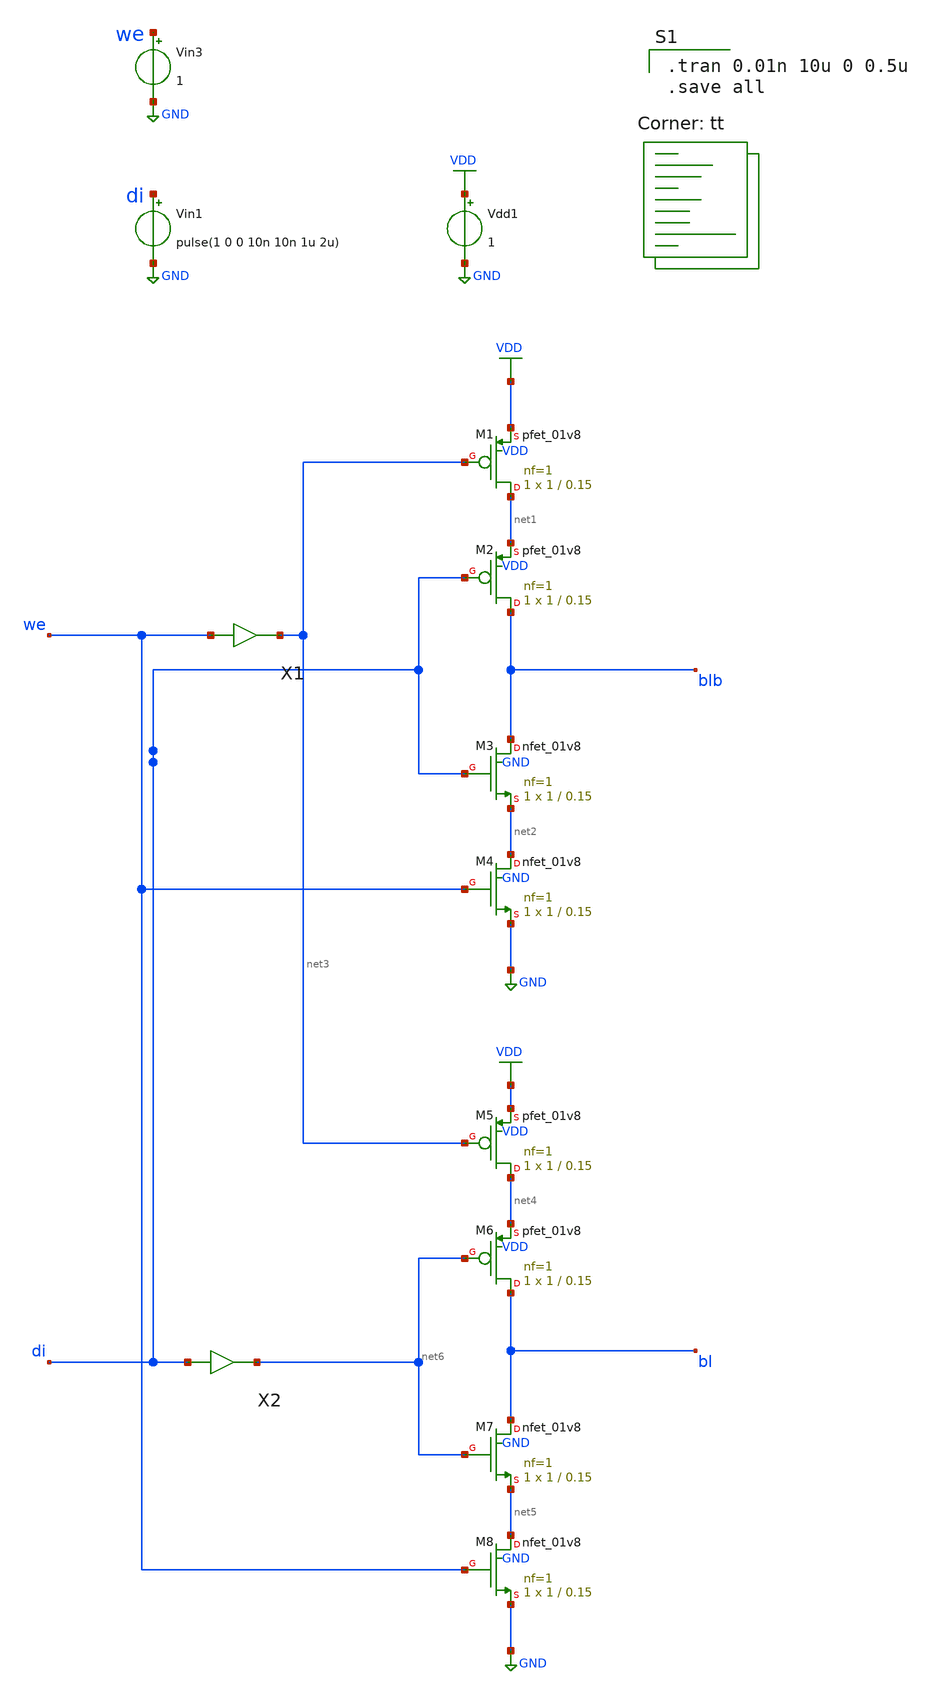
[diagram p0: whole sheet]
** sch_path: gates/Memory/write drive sim.sch
**.subckt write drive sim
X1 we net3 inv_vtc
X2 di net6 inv_vtc
XM1 net1 net3 VDD VDD sky130_fd_pr__pfet_01v8 L=0.15 W=1 nf=1 ad='int((nf+1)/2) * W/nf * 0.29' as='int((nf+2)/2) * W/nf * 0.29'
+ pd='2*int((nf+1)/2) * (W/nf + 0.29)' ps='2*int((nf+2)/2) * (W/nf + 0.29)' nrd='0.29 / W' nrs='0.29 / W'
+ sa=0 sb=0 sd=0 mult=1 m=1
XM2 blb di net1 VDD sky130_fd_pr__pfet_01v8 L=0.15 W=1 nf=1 ad='int((nf+1)/2) * W/nf * 0.29' as='int((nf+2)/2) * W/nf * 0.29'
+ pd='2*int((nf+1)/2) * (W/nf + 0.29)' ps='2*int((nf+2)/2) * (W/nf + 0.29)' nrd='0.29 / W' nrs='0.29 / W'
+ sa=0 sb=0 sd=0 mult=1 m=1
XM3 blb di net2 GND sky130_fd_pr__nfet_01v8 L=0.15 W=1 nf=1 ad='int((nf+1)/2) * W/nf * 0.29' as='int((nf+2)/2) * W/nf * 0.29'
+ pd='2*int((nf+1)/2) * (W/nf + 0.29)' ps='2*int((nf+2)/2) * (W/nf + 0.29)' nrd='0.29 / W' nrs='0.29 / W'
+ sa=0 sb=0 sd=0 mult=1 m=1
XM4 net2 we GND GND sky130_fd_pr__nfet_01v8 L=0.15 W=1 nf=1 ad='int((nf+1)/2) * W/nf * 0.29' as='int((nf+2)/2) * W/nf * 0.29'
+ pd='2*int((nf+1)/2) * (W/nf + 0.29)' ps='2*int((nf+2)/2) * (W/nf + 0.29)' nrd='0.29 / W' nrs='0.29 / W'
+ sa=0 sb=0 sd=0 mult=1 m=1
XM5 net4 net3 VDD VDD sky130_fd_pr__pfet_01v8 L=0.15 W=1 nf=1 ad='int((nf+1)/2) * W/nf * 0.29' as='int((nf+2)/2) * W/nf * 0.29'
+ pd='2*int((nf+1)/2) * (W/nf + 0.29)' ps='2*int((nf+2)/2) * (W/nf + 0.29)' nrd='0.29 / W' nrs='0.29 / W'
+ sa=0 sb=0 sd=0 mult=1 m=1
XM6 bl net6 net4 VDD sky130_fd_pr__pfet_01v8 L=0.15 W=1 nf=1 ad='int((nf+1)/2) * W/nf * 0.29' as='int((nf+2)/2) * W/nf * 0.29'
+ pd='2*int((nf+1)/2) * (W/nf + 0.29)' ps='2*int((nf+2)/2) * (W/nf + 0.29)' nrd='0.29 / W' nrs='0.29 / W'
+ sa=0 sb=0 sd=0 mult=1 m=1
XM7 bl net6 net5 GND sky130_fd_pr__nfet_01v8 L=0.15 W=1 nf=1 ad='int((nf+1)/2) * W/nf * 0.29' as='int((nf+2)/2) * W/nf * 0.29'
+ pd='2*int((nf+1)/2) * (W/nf + 0.29)' ps='2*int((nf+2)/2) * (W/nf + 0.29)' nrd='0.29 / W' nrs='0.29 / W'
+ sa=0 sb=0 sd=0 mult=1 m=1
XM8 net5 we GND GND sky130_fd_pr__nfet_01v8 L=0.15 W=1 nf=1 ad='int((nf+1)/2) * W/nf * 0.29' as='int((nf+2)/2) * W/nf * 0.29'
+ pd='2*int((nf+1)/2) * (W/nf + 0.29)' ps='2*int((nf+2)/2) * (W/nf + 0.29)' nrd='0.29 / W' nrs='0.29 / W'
+ sa=0 sb=0 sd=0 mult=1 m=1
Vdd1 VDD GND 1
Vin1 di GND pulse(1 0 0 10n 10n 1u 2u)
Vin3 we GND 1
**** begin user architecture code

.tran 0.01n 10u 0 0.5u
.save all

.lib $::SKYWATER_MODELS/sky130.lib.spice tt
**** end user architecture code
**.ends

* expanding   symbol:  /home/apn/test_xschem_sky130/inv_vtc.sym # of pins=2
** sym_path: gates/Memory/inv_vtc.sym
** sch_path: gates/Memory/inv_vtc.sch
.subckt inv_vtc A Y
*.ipin A
*.opin Y
XM1 Y A VDD VDD sky130_fd_pr__pfet_01v8 L=0.15 W=2 nf=1 ad='int((nf+1)/2) * W/nf * 0.29' as='int((nf+2)/2) * W/nf * 0.29'
+ pd='2*int((nf+1)/2) * (W/nf + 0.29)' ps='2*int((nf+2)/2) * (W/nf + 0.29)' nrd='0.29 / W' nrs='0.29 / W'
+ sa=0 sb=0 sd=0 mult=1 m=1
XM2 Y A GND GND sky130_fd_pr__nfet_01v8 L=0.15 W=1 nf=1 ad='int((nf+1)/2) * W/nf * 0.29' as='int((nf+2)/2) * W/nf * 0.29'
+ pd='2*int((nf+1)/2) * (W/nf + 0.29)' ps='2*int((nf+2)/2) * (W/nf + 0.29)' nrd='0.29 / W' nrs='0.29 / W'
+ sa=0 sb=0 sd=0 mult=1 m=1
.ends

.GLOBAL GND
.GLOBAL VDD
.end
